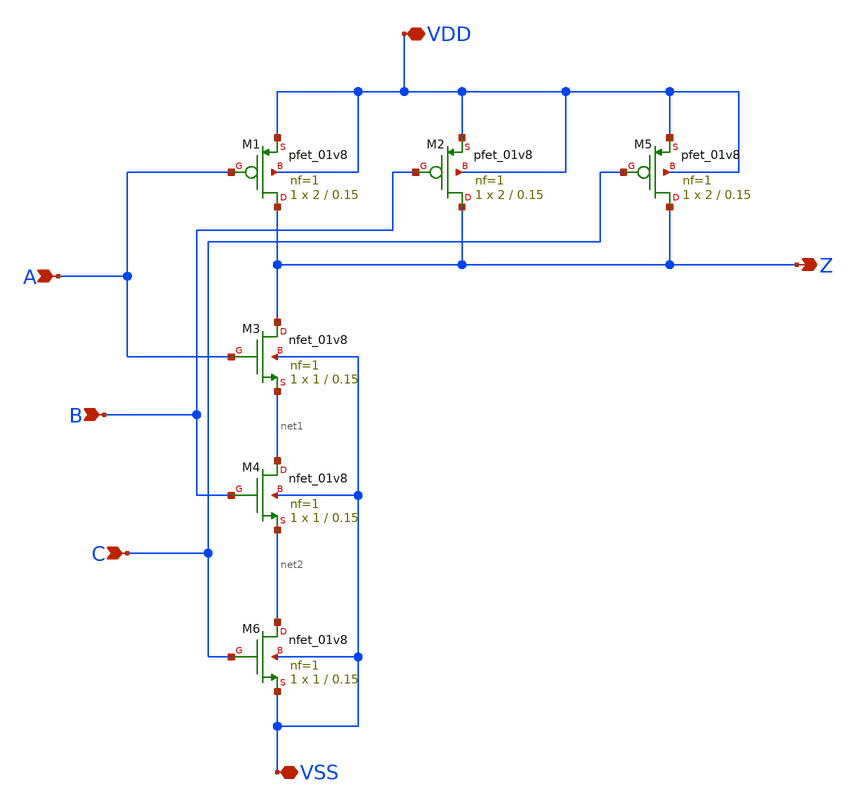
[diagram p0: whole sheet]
** sch_path: 3INPUTNAND1.sch
**.subckt 3INPUTNAND1 A B VDD VSS Z C
*.ipin A
*.ipin B
*.iopin VDD
*.iopin VSS
*.opin Z
*.ipin C
XM1 Z A VDD VDD sky130_fd_pr__pfet_01v8 L=0.15 W=2 nf=1 ad='int((1 + 1)/2) * 2 / 1 * 0.29' as='int((1 + 2)/2) * 2 / 1 * 0.29'
+ pd='2*int((1 + 1)/2) * (2 / 1 + 0.29)' ps='2*int((1 + 2)/2) * (2 / 1 + 0.29)' nrd='0.29 / 2 ' nrs='0.29 / 2 '
+ sa=0 sb=0 sd=0 mult=1 m=1
XM2 Z B VDD VDD sky130_fd_pr__pfet_01v8 L=0.15 W=2 nf=1 ad='int((1 + 1)/2) * 2 / 1 * 0.29' as='int((1 + 2)/2) * 2 / 1 * 0.29'
+ pd='2*int((1 + 1)/2) * (2 / 1 + 0.29)' ps='2*int((1 + 2)/2) * (2 / 1 + 0.29)' nrd='0.29 / 2 ' nrs='0.29 / 2 '
+ sa=0 sb=0 sd=0 mult=1 m=1
XM3 Z A net1 VSS sky130_fd_pr__nfet_01v8 L=0.15 W=1 nf=1 ad='int((1 + 1)/2) * 1 / 1 * 0.29' as='int((1 + 2)/2) * 1 / 1 * 0.29'
+ pd='2*int((1 + 1)/2) * (1 / 1 + 0.29)' ps='2*int((1 + 2)/2) * (1 / 1 + 0.29)' nrd='0.29 / 1 ' nrs='0.29 / 1 '
+ sa=0 sb=0 sd=0 mult=1 m=1
XM4 net1 B net2 VSS sky130_fd_pr__nfet_01v8 L=0.15 W=1 nf=1 ad='int((1 + 1)/2) * 1 / 1 * 0.29' as='int((1 + 2)/2) * 1 / 1 * 0.29'
+ pd='2*int((1 + 1)/2) * (1 / 1 + 0.29)' ps='2*int((1 + 2)/2) * (1 / 1 + 0.29)' nrd='0.29 / 1 ' nrs='0.29 / 1 '
+ sa=0 sb=0 sd=0 mult=1 m=1
XM5 Z C VDD VDD sky130_fd_pr__pfet_01v8 L=0.15 W=2 nf=1 ad='int((1 + 1)/2) * 2 / 1 * 0.29' as='int((1 + 2)/2) * 2 / 1 * 0.29'
+ pd='2*int((1 + 1)/2) * (2 / 1 + 0.29)' ps='2*int((1 + 2)/2) * (2 / 1 + 0.29)' nrd='0.29 / 2 ' nrs='0.29 / 2 '
+ sa=0 sb=0 sd=0 mult=1 m=1
XM6 net2 C VSS VSS sky130_fd_pr__nfet_01v8 L=0.15 W=1 nf=1 ad='int((1 + 1)/2) * 1 / 1 * 0.29' as='int((1 + 2)/2) * 1 / 1 * 0.29'
+ pd='2*int((1 + 1)/2) * (1 / 1 + 0.29)' ps='2*int((1 + 2)/2) * (1 / 1 + 0.29)' nrd='0.29 / 1 ' nrs='0.29 / 1 '
+ sa=0 sb=0 sd=0 mult=1 m=1
**.ends
.end
